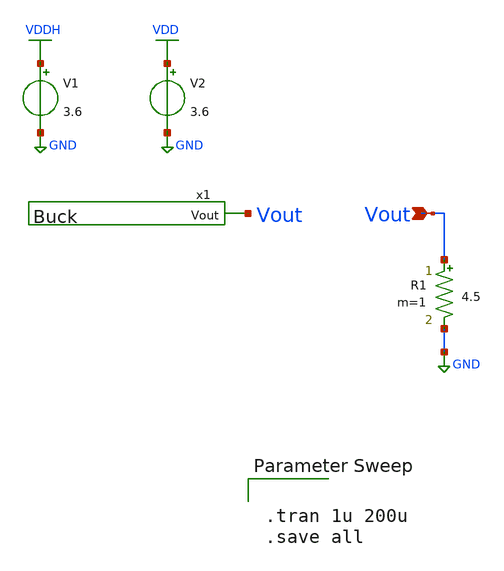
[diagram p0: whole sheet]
** sch_path: Ene_Thompson/test_Buck.sch
**.subckt test_Buck Vout
*.ipin Vout
x1 Vout Buck
V1 VDDH GND 3.6
R1 Vout GND 4.5 m=1
V2 VDD GND 3.6
**** begin user architecture code

.lib $::SKYWATER_MODELS/sky130.lib.spice tt


.tran 1u 200u
.save all



.subckt sky130_fd_sc_hd__nand2_1 A B VGND VNB VPB VPWR Y
X0 Y A VPWR VPB sky130_fd_pr__pfet_g5v0d10v5 w=1 l=0.5
X1 VPWR B Y VPB sky130_fd_pr__pfet_g5v0d10v5 w=1 l=0.5
X2 VGND B a_113_47# VNB sky130_fd_pr__nfet_g5v0d10v5 w=1 l=0.5
X3 a_113_47# A Y VNB sky130_fd_pr__nfet_g5v0d10v5 w=1 l=0.5
.ends

.subckt sky130_fd_sc_hd__inv_1 A VGND VNB VPB VPWR Y
X0 VGND A Y VNB sky130_fd_pr__nfet_g5v0d10v5 w=1 l=0.5
X1 VPWR A Y VPB sky130_fd_pr__pfet_g5v0d10v5 w=1 l=0.5
.ends

VVPWR VDD VPWR 0
VVPB VDD VPB 0
VVGND GND VGND 0
VVNB GND VGND 0

.GLOBAL VPWR
.GLOBAL VPB
.GLOBAL VNB
.GLOBAL VGND

**** end user architecture code
**.ends

* expanding   symbol:  Buck.sym # of pins=1
** sym_path: Ene_Thompson/Buck.sym
** sch_path: Ene_Thompson/Buck.sch
.subckt Buck Vout
*.opin Vout
XM1 vl net6 net1 VDDH sky130_fd_pr__pfet_g5v0d10v5 L=0.5 W=20 nf=1 ad='int((nf+1)/2) * W/nf * 0.29' as='int((nf+2)/2) * W/nf * 0.29'
+ pd='2*int((nf+1)/2) * (W/nf + 0.29)' ps='2*int((nf+2)/2) * (W/nf + 0.29)' nrd='0.29 / W' nrs='0.29 / W'
+ sa=0 sb=0 sd=0 mult=1025 m=1025
Xx3 vl net5 net4 GND sky130_fd_pr__nfet_g5v0d10v5 L=0.5 W=20 nf=1 ad='int((nf+1)/2) * W/nf * 0.29' as='int((nf+2)/2) * W/nf * 0.29'
+ pd='2*int((nf+1)/2) * (W/nf + 0.29)' ps='2*int((nf+2)/2) * (W/nf + 0.29)' nrd='0.29 / W' nrs='0.29 / W'
+ sa=0 sb=0 sd=0 mult=975 m=975
L1 net3 Vout 4.7u m=1
C1 Vout net2 1u m=1
R1 vl net3 1.5m m=1
R2 GND net2 10m m=1
Vm1 VDDH net1 0
.save i(vm1)
Vm2 net4 GND 0
.save i(vm2)
x1 pswitch net6 drive_train
x2 nswitch net5 drive_train
V2 pwm GND PULSE(0 3.6 0 0.01u 0.01u 0.5u 1u)
x4 pswitch pwm nswitch deadtime
.ends


* expanding   symbol:  drive_train.sym # of pins=2
** sym_path: Ene_Thompson/drive_train.sym
** sch_path: Ene_Thompson/drive_train.sch
.subckt drive_train A Y
*.opin Y
*.ipin A
XM1 net1 A GND GND sky130_fd_pr__nfet_g5v0d10v5 L=0.5 W=1 nf=1 ad='int((nf+1)/2) * W/nf * 0.29' as='int((nf+2)/2) * W/nf * 0.29'
+ pd='2*int((nf+1)/2) * (W/nf + 0.29)' ps='2*int((nf+2)/2) * (W/nf + 0.29)' nrd='0.29 / W' nrs='0.29 / W'
+ sa=0 sb=0 sd=0 mult=7 m=7
XM2 net1 A VDD VDD sky130_fd_pr__pfet_g5v0d10v5 L=0.5 W=1 nf=1 ad='int((nf+1)/2) * W/nf * 0.29' as='int((nf+2)/2) * W/nf * 0.29'
+ pd='2*int((nf+1)/2) * (W/nf + 0.29)' ps='2*int((nf+2)/2) * (W/nf + 0.29)' nrd='0.29 / W' nrs='0.29 / W'
+ sa=0 sb=0 sd=0 mult=7 m=7
XM3 net2 net1 GND GND sky130_fd_pr__nfet_g5v0d10v5 L=0.5 W=1 nf=1 ad='int((nf+1)/2) * W/nf * 0.29' as='int((nf+2)/2) * W/nf * 0.29'
+ pd='2*int((nf+1)/2) * (W/nf + 0.29)' ps='2*int((nf+2)/2) * (W/nf + 0.29)' nrd='0.29 / W' nrs='0.29 / W'
+ sa=0 sb=0 sd=0 mult=50 m=50
XM4 net2 net1 VDD VDD sky130_fd_pr__pfet_g5v0d10v5 L=0.5 W=1 nf=1 ad='int((nf+1)/2) * W/nf * 0.29' as='int((nf+2)/2) * W/nf * 0.29'
+ pd='2*int((nf+1)/2) * (W/nf + 0.29)' ps='2*int((nf+2)/2) * (W/nf + 0.29)' nrd='0.29 / W' nrs='0.29 / W'
+ sa=0 sb=0 sd=0 mult=50 m=50
XM5 net3 net2 GND GND sky130_fd_pr__nfet_g5v0d10v5 L=0.5 W=10 nf=1 ad='int((nf+1)/2) * W/nf * 0.29' as='int((nf+2)/2) * W/nf * 0.29'
+ pd='2*int((nf+1)/2) * (W/nf + 0.29)' ps='2*int((nf+2)/2) * (W/nf + 0.29)' nrd='0.29 / W' nrs='0.29 / W'
+ sa=0 sb=0 sd=0 mult=35 m=35
XM6 net3 net2 VDD VDD sky130_fd_pr__pfet_g5v0d10v5 L=0.5 W=10 nf=1 ad='int((nf+1)/2) * W/nf * 0.29' as='int((nf+2)/2) * W/nf * 0.29'
+ pd='2*int((nf+1)/2) * (W/nf + 0.29)' ps='2*int((nf+2)/2) * (W/nf + 0.29)' nrd='0.29 / W' nrs='0.29 / W'
+ sa=0 sb=0 sd=0 mult=35 m=35
XM7 Y net3 GND GND sky130_fd_pr__nfet_g5v0d10v5 L=0.5 W=20 nf=1 ad='int((nf+1)/2) * W/nf * 0.29' as='int((nf+2)/2) * W/nf * 0.29'
+ pd='2*int((nf+1)/2) * (W/nf + 0.29)' ps='2*int((nf+2)/2) * (W/nf + 0.29)' nrd='0.29 / W' nrs='0.29 / W'
+ sa=0 sb=0 sd=0 mult=125 m=125
XM8 Y net3 VDD VDD sky130_fd_pr__pfet_g5v0d10v5 L=0.5 W=20 nf=1 ad='int((nf+1)/2) * W/nf * 0.29' as='int((nf+2)/2) * W/nf * 0.29'
+ pd='2*int((nf+1)/2) * (W/nf + 0.29)' ps='2*int((nf+2)/2) * (W/nf + 0.29)' nrd='0.29 / W' nrs='0.29 / W'
+ sa=0 sb=0 sd=0 mult=125 m=125
.ends


* expanding   symbol:  deadtime.sym # of pins=3
** sym_path: Ene_Thompson/deadtime.sym
** sch_path: Ene_Thompson/deadtime.sch
.subckt deadtime highside pwm lowside
*.ipin pwm
*.opin highside
*.opin lowside
x1 pwm low_fb VGND VNB VPB VPWR high1 sky130_fd_sc_hd__nand2_1
x2 high_fb pwm_n VGND VNB VPB VPWR low1 sky130_fd_sc_hd__nand2_1
x3 high1 VGND VNB VPB VPWR high2 sky130_fd_sc_hd__inv_1
x4 high2 VGND VNB VPB VPWR high3 sky130_fd_sc_hd__inv_1
x5 high3 VGND VNB VPB VPWR highside sky130_fd_sc_hd__inv_1
x6 highside VGND VNB VPB VPWR high_fb sky130_fd_sc_hd__inv_1
x7 low1 VGND VNB VPB VPWR low2 sky130_fd_sc_hd__inv_1
x8 low2 VGND VNB VPB VPWR lowside sky130_fd_sc_hd__inv_1
x9 lowside VGND VNB VPB VPWR low4 sky130_fd_sc_hd__inv_1
x10 low4 VGND VNB VPB VPWR low_fb sky130_fd_sc_hd__inv_1
x11 pwm VGND VNB VPB VPWR pwm_n sky130_fd_sc_hd__inv_1
.ends

.GLOBAL VDDH
.GLOBAL GND
.GLOBAL VDD
.end
